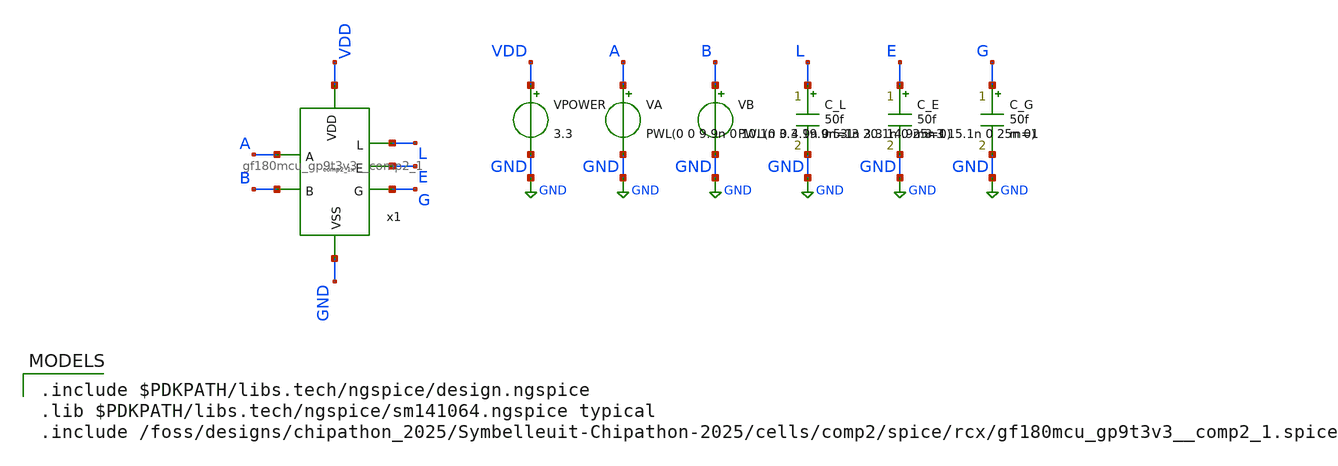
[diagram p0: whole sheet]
** sch_path: cells/comp2/cace/templates/comp2_tb_dynamic.sch
**.subckt comp2_tb_dynamic
x1 VDD L A E G B GND gf180mcu_gp9t3v3__comp2_1
VPOWER VDD GND 3.3
.save i(vpower)
VA A GND PWL(0 0 9.9n 0 10.1n 3.3 19.9n 3.3 20.1n 0 25n 0)
VB B GND PWL(0 0 4.9n 0 5.1n 3.3 14.9n 3.3 15.1n 0 25n 0)
C_L L GND 50f m=1
C_E E GND 50f m=1
C_G G GND 50f m=1
**** begin user architecture code

.include $PDKPATH/libs.tech/ngspice/design.ngspice
.lib $PDKPATH/libs.tech/ngspice/sm141064.ngspice typical
.include /foss/designs/chipathon_2025/Symbelleuit-Chipathon-2025/cells/comp2/spice/rcx/gf180mcu_gp9t3v3__comp2_1.spice


* CACE Peak Dynamic Current Simulation
.tran 100p 25n
.control
  run
  let idd = -i(VPOWER)
  meas tran i_peak MAX idd from=1n to=25n
  print i_peak
  echo $&i_peak > comp2_tb_dynamic_0.data
.endc
.GLOBAL GND


**** end user architecture code
**.ends
.GLOBAL GND
.end
